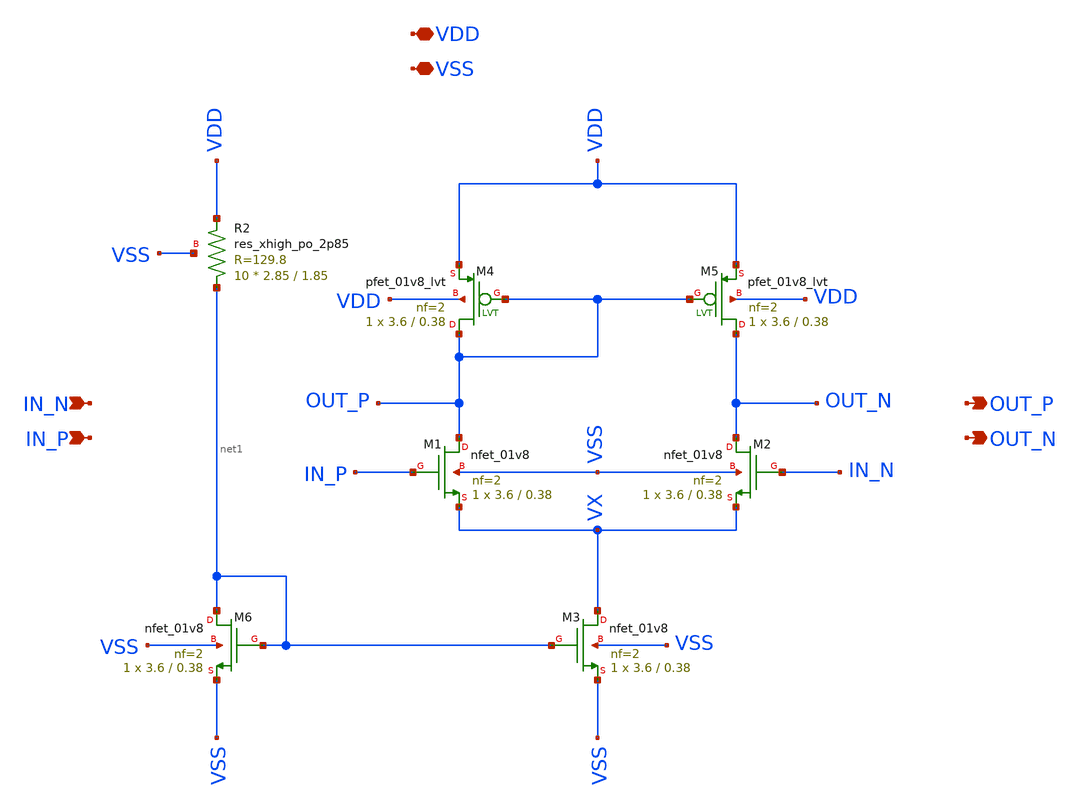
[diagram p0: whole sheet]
** sch_path: xschem/diff_amp.sch
**.subckt diff_amp VDD VSS IN_N IN_P OUT_P OUT_N
*.iopin VDD
*.iopin VSS
*.ipin IN_N
*.ipin IN_P
*.opin OUT_P
*.opin OUT_N
XM6 net1 net1 VSS VSS sky130_fd_pr__nfet_01v8 L=0.38 W=3.6 nf=2 ad='int((nf+1)/2) * W/nf * 0.29' as='int((nf+2)/2) * W/nf * 0.29'
+ pd='2*int((nf+1)/2) * (W/nf + 0.29)' ps='2*int((nf+2)/2) * (W/nf + 0.29)' nrd='0.29 / W' nrs='0.29 / W'
+ sa=0 sb=0 sd=0 mult=1 m=1
XM4 OUT_P OUT_P VDD VDD sky130_fd_pr__pfet_01v8_lvt L=0.38 W=3.6 nf=2 ad='int((nf+1)/2) * W/nf * 0.29'
+ as='int((nf+2)/2) * W/nf * 0.29' pd='2*int((nf+1)/2) * (W/nf + 0.29)' ps='2*int((nf+2)/2) * (W/nf + 0.29)'
+ nrd='0.29 / W' nrs='0.29 / W' sa=0 sb=0 sd=0 mult=1 m=1
XR2 net1 VDD VSS sky130_fd_pr__res_xhigh_po_2p85 L=1.85 mult=10 m=10
XM3 VX net1 VSS VSS sky130_fd_pr__nfet_01v8 L=0.38 W=3.6 nf=2 ad='int((nf+1)/2) * W/nf * 0.29' as='int((nf+2)/2) * W/nf * 0.29'
+ pd='2*int((nf+1)/2) * (W/nf + 0.29)' ps='2*int((nf+2)/2) * (W/nf + 0.29)' nrd='0.29 / W' nrs='0.29 / W'
+ sa=0 sb=0 sd=0 mult=1 m=1
XM1 OUT_P IN_P VX VSS sky130_fd_pr__nfet_01v8 L=0.38 W=3.6 nf=2 ad='int((nf+1)/2) * W/nf * 0.29' as='int((nf+2)/2) * W/nf * 0.29'
+ pd='2*int((nf+1)/2) * (W/nf + 0.29)' ps='2*int((nf+2)/2) * (W/nf + 0.29)' nrd='0.29 / W' nrs='0.29 / W'
+ sa=0 sb=0 sd=0 mult=1 m=1
XM2 OUT_N IN_N VX VSS sky130_fd_pr__nfet_01v8 L=0.38 W=3.6 nf=2 ad='int((nf+1)/2) * W/nf * 0.29' as='int((nf+2)/2) * W/nf * 0.29'
+ pd='2*int((nf+1)/2) * (W/nf + 0.29)' ps='2*int((nf+2)/2) * (W/nf + 0.29)' nrd='0.29 / W' nrs='0.29 / W'
+ sa=0 sb=0 sd=0 mult=1 m=1
XM5 OUT_N OUT_P VDD VDD sky130_fd_pr__pfet_01v8_lvt L=0.38 W=3.6 nf=2 ad='int((nf+1)/2) * W/nf * 0.29'
+ as='int((nf+2)/2) * W/nf * 0.29' pd='2*int((nf+1)/2) * (W/nf + 0.29)' ps='2*int((nf+2)/2) * (W/nf + 0.29)'
+ nrd='0.29 / W' nrs='0.29 / W' sa=0 sb=0 sd=0 mult=1 m=1
**.ends
.end
